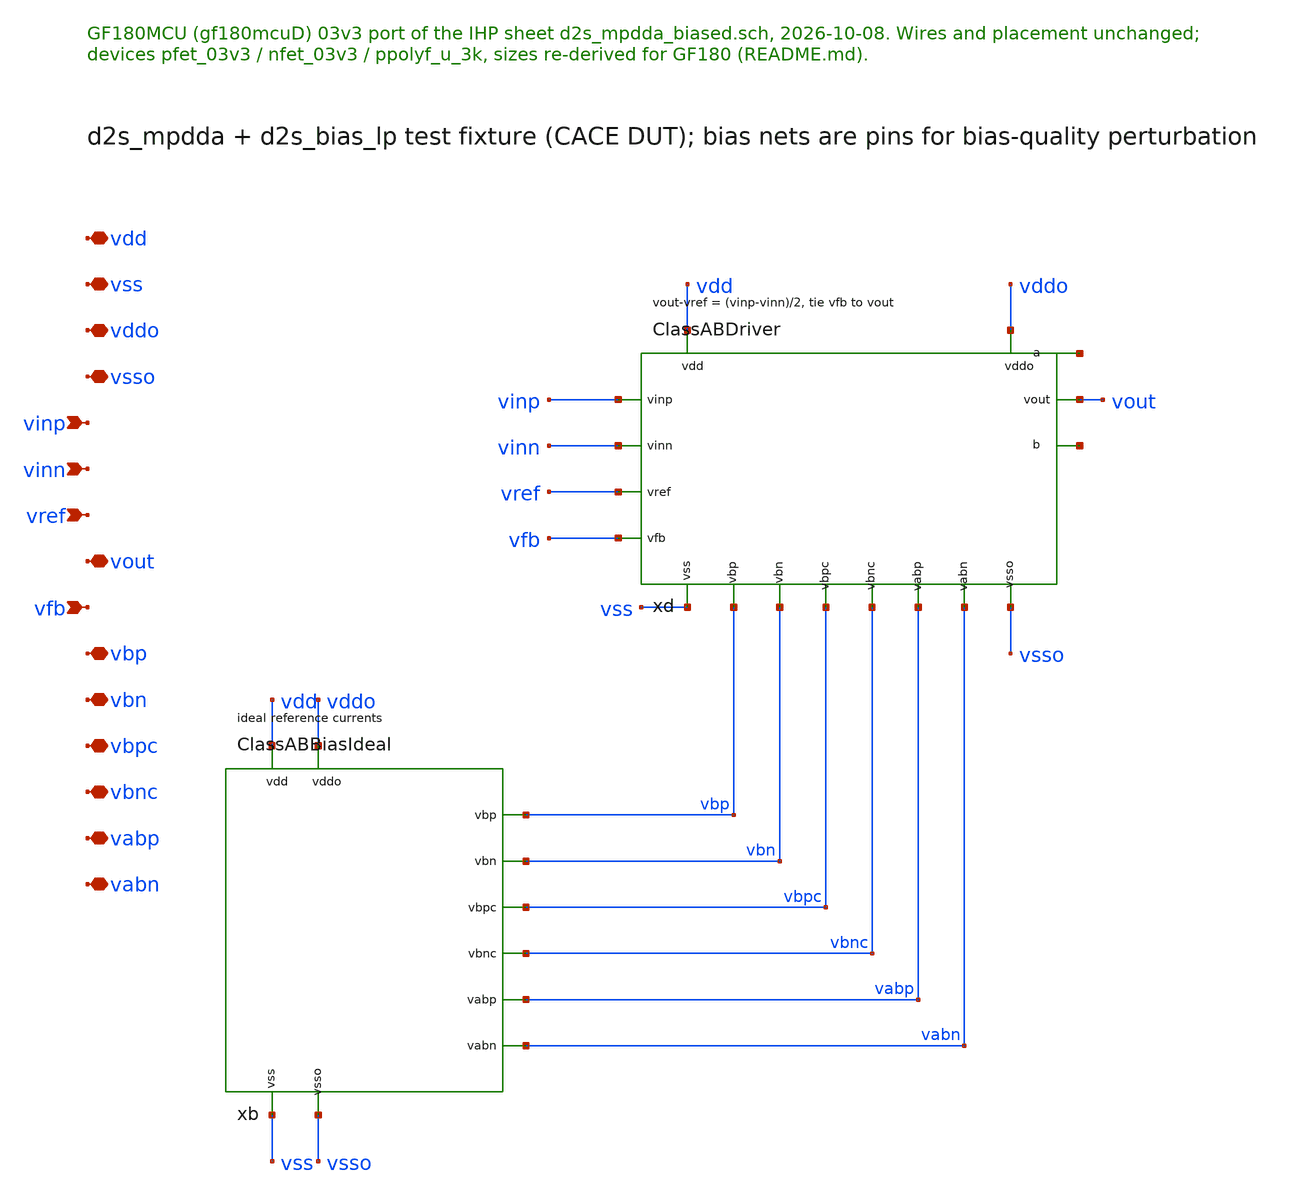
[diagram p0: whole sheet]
** sch_path: macros/ClassABDriver/schematic/xschem/ClassABDriverBiased.sch
**.subckt ClassABDriverBiased vdd vss vddo vsso vinp vinn vref vout vfb vbp vbn vbpc vbnc vabp vabn
*.iopin vdd
*.iopin vss
*.iopin vddo
*.iopin vsso
*.ipin vinp
*.ipin vinn
*.ipin vref
*.iopin vout
*.ipin vfb
*.iopin vbp
*.iopin vbn
*.iopin vbpc
*.iopin vbnc
*.iopin vabp
*.iopin vabn
xd vdd vss vddo vsso vinp vinn vref vout vfb vbp vbn vbpc vbnc vabp vabn net1 net2 ClassABDriver
xb vdd vss vddo vsso vbp vbn vbpc vbnc vabp vabn ClassABBiasIdeal
**.ends
.end
